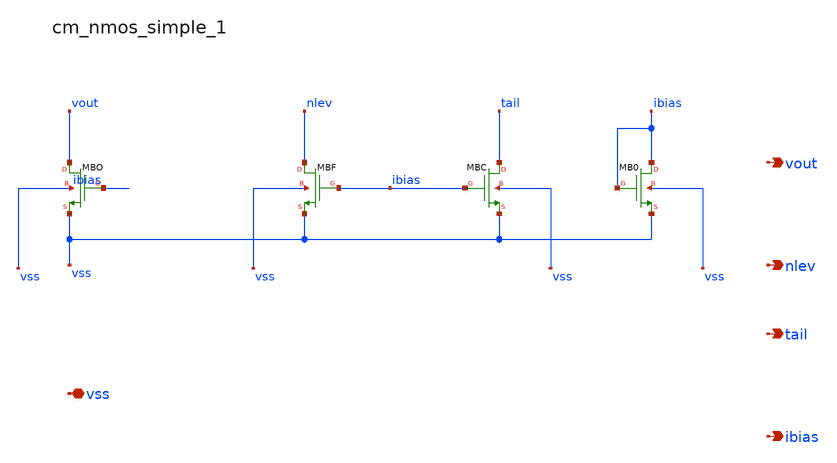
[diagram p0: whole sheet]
** sch_path: analog-db/raw/amp_032_ti_ldo_error_selfbias/hier/blocks/cm_nmos_simple_1.sch
**.subckt cm_nmos_simple_1 vss vout nlev tail ibias
*.iopin vss
*.opin vout
*.opin nlev
*.opin tail
*.opin ibias
XMB0 ibias ibias vss vss sg13_lv_nmos w=x_dut_xmb0_w l=x_dut_xmb0_l ng=1 m=1
XMBC tail ibias vss vss sg13_lv_nmos w=x_dut_xmbc_w l=x_dut_xmbc_l ng=1 m=x_dut_xmbc_m
XMBF nlev ibias vss vss sg13_lv_nmos w=x_dut_xmbf_w l=x_dut_xmbf_l ng=1 m=1
XMBO vout ibias vss vss sg13_lv_nmos w=x_dut_xmbo_w l=x_dut_xmbo_l ng=1 m=x_dut_xmbo_m
**.ends
.end
